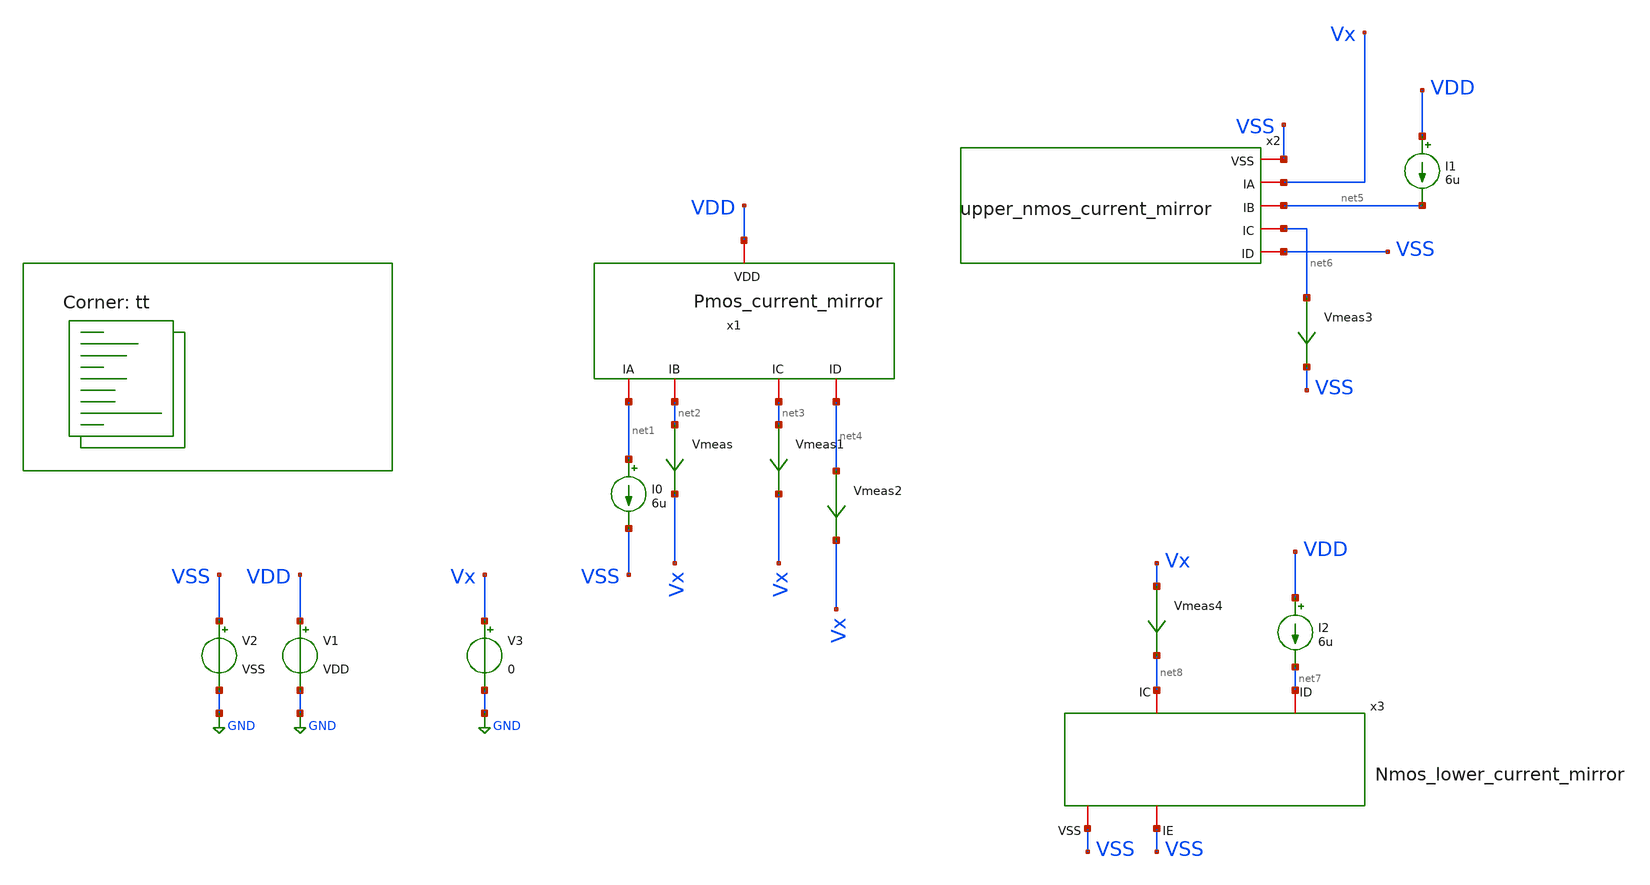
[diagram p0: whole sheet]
** sch_path: Learning/single_ended_amplifiers/VA001_series/Design_and_Analysis_of_Two-Stage_CMOS_Operational_Amplifier_for_Fluorescence_Signal_Processing_sky130_5V/amplifier_design/test.sch
**.subckt test
V1 VDD GND VDD
V2 VSS GND VSS
x1 VDD net1 net2 net3 net4 Pmos_current_mirror
I0 net1 VSS 6u
V3 Vx GND 0
Vmeas net2 Vx 0
.save i(vmeas)
Vmeas1 net3 Vx 0
.save i(vmeas1)
Vmeas2 net4 Vx 0
.save i(vmeas2)
I1 VDD net5 6u
Vmeas3 net6 VSS 0
.save i(vmeas3)
x2 VSS Vx net5 net6 VSS upper_nmos_current_mirror
x3 VSS net8 net7 VSS Nmos_lower_current_mirror
I2 VDD net7 6u
Vmeas4 Vx net8 0
.save i(vmeas4)
**** begin user architecture code
.lib $::SKYWATER_MODELS/sky130.lib.spice tt

.Temp 27
.param VDD = 5
.param VSS = 0
.param VCM = 2.5
.param VCM_NEG={-VCM}
.param V_OFF = -880.69u
.param CL = 3p


.control
save all

dc V3 0 5 0.001
plot i(Vmeas4)

.endc



.subckt upper_nmos_current_mirror VSS IA IB IC ID
X0 VSS VSS IB VSS sky130_fd_pr__nfet_g5v0d10v5 ad=0.29 pd=2.58 as=0.145 ps=1.29 w=1 l=2
X1 VSS VSS ID VSS sky130_fd_pr__nfet_g5v0d10v5 ad=0.145 pd=1.29 as=0.145 ps=1.29 w=1 l=2
X2 IA IB IC VSS sky130_fd_pr__nfet_g5v0d10v5 ad=0.145 pd=1.29 as=0.145 ps=1.29 w=1 l=2
X3 IB IB ID VSS sky130_fd_pr__nfet_g5v0d10v5 ad=0.145 pd=1.29 as=0.145 ps=1.29 w=1 l=2
X4 VSS VSS IA VSS sky130_fd_pr__nfet_g5v0d10v5 ad=0.145 pd=1.29 as=0.145 ps=1.29 w=1 l=2
X5 IA VSS VSS VSS sky130_fd_pr__nfet_g5v0d10v5 ad=0.145 pd=1.29 as=0.145 ps=1.29 w=1 l=2
X6 ID IB IB VSS sky130_fd_pr__nfet_g5v0d10v5 ad=0.145 pd=1.29 as=0.145 ps=1.29 w=1 l=2
X7 IB VSS VSS VSS sky130_fd_pr__nfet_g5v0d10v5 ad=0.145 pd=1.29 as=0.29 ps=2.58 w=1 l=2
X8 IC IB IA VSS sky130_fd_pr__nfet_g5v0d10v5 ad=0.145 pd=1.29 as=0.145 ps=1.29 w=1 l=2
X9 ID VSS VSS VSS sky130_fd_pr__nfet_g5v0d10v5 ad=0.145 pd=1.29 as=0.145 ps=1.29 w=1 l=2
X10 VSS VSS IB VSS sky130_fd_pr__nfet_g5v0d10v5 ad=2.32 pd=20.64 as=1.16 ps=10.32 w=1 l=2
X11 VSS VSS ID VSS sky130_fd_pr__nfet_g5v0d10v5 ad=0 pd=0 as=1.16 ps=10.32 w=1 l=2
X12 IA IB IC VSS sky130_fd_pr__nfet_g5v0d10v5 ad=1.16 pd=10.32 as=0.58 ps=5.16 w=1 l=2
X13 IB IB ID VSS sky130_fd_pr__nfet_g5v0d10v5 ad=0 pd=0 as=0 ps=0 w=1 l=2
X14 VSS VSS IA VSS sky130_fd_pr__nfet_g5v0d10v5 ad=0 pd=0 as=0 ps=0 w=1 l=2
X15 IA VSS VSS VSS sky130_fd_pr__nfet_g5v0d10v5 ad=0 pd=0 as=0 ps=0 w=1 l=2
X16 ID IB IB VSS sky130_fd_pr__nfet_g5v0d10v5 ad=0 pd=0 as=0 ps=0 w=1 l=2
X17 IB VSS VSS VSS sky130_fd_pr__nfet_g5v0d10v5 ad=0 pd=0 as=0 ps=0 w=1 l=2
X18 IC IB IA VSS sky130_fd_pr__nfet_g5v0d10v5 ad=0 pd=0 as=0 ps=0 w=1 l=2
X19 ID VSS VSS VSS sky130_fd_pr__nfet_g5v0d10v5 ad=0 pd=0 as=0 ps=0 w=1 l=2
C0 IB VSS 2.32803f
C1 VSS 0 7.91723f
C2 IB 0 7.85092f
.ends




.subckt pmos_current_mirror VDD IA IB IC ID
X0 IA VDD VDD VDD sky130_fd_pr__pfet_g5v0d10v5 ad=0.29 pd=2.58 as=0.29 ps=2.58 w=1 l=2.2
X1 IA VDD VDD VDD sky130_fd_pr__pfet_g5v0d10v5 ad=1.16003 pd=10.325 as=9.86003 ps=87.725 w=1 l=2.2
X2 VDD VDD VDD VDD sky130_fd_pr__pfet_g5v0d10v5 ad=0 pd=0 as=0 ps=0 w=1 l=2.2
X3 VDD IA IA VDD sky130_fd_pr__pfet_g5v0d10v5 ad=0.29 pd=2.58 as=0.29 ps=2.58 w=1 l=2
X4 VDD IA IA VDD sky130_fd_pr__pfet_g5v0d10v5 ad=0 pd=0 as=0 ps=0 w=1 l=2
X5 VDD IA IA VDD sky130_fd_pr__pfet_g5v0d10v5 ad=0 pd=0 as=0 ps=0 w=1 l=2
X6 VDD IA IA VDD sky130_fd_pr__pfet_g5v0d10v5 ad=0 pd=0 as=0 ps=0 w=1 l=2
X7 VDD IA IB VDD sky130_fd_pr__pfet_g5v0d10v5 ad=0.29 pd=2.58 as=0.145 ps=1.29 w=1 l=2.2
X8 IB IA VDD VDD sky130_fd_pr__pfet_g5v0d10v5 ad=0.145 pd=1.29 as=0.29 ps=2.58 w=1 l=2.2
X9 VDD IA ID VDD sky130_fd_pr__pfet_g5v0d10v5 ad=0.29 pd=2.58 as=0.145 ps=1.29 w=1 l=2.2
X10 ID IA VDD VDD sky130_fd_pr__pfet_g5v0d10v5 ad=0.145 pd=1.29 as=0.145 ps=1.29 w=1 l=2.2
X11 VDD IA ID VDD sky130_fd_pr__pfet_g5v0d10v5 ad=0.145 pd=1.29 as=0.145 ps=1.29 w=1 l=2.2
X12 ID IA VDD VDD sky130_fd_pr__pfet_g5v0d10v5 ad=0.145 pd=1.29 as=0.29 ps=2.58 w=1 l=2.2
X13 VDD IA IB VDD sky130_fd_pr__pfet_g5v0d10v5 ad=0 pd=0 as=0.58 ps=5.16 w=1 l=2.2
X14 IB IA VDD VDD sky130_fd_pr__pfet_g5v0d10v5 ad=0 pd=0 as=0 ps=0 w=1 l=2.2
X15 VDD IA IC VDD sky130_fd_pr__pfet_g5v0d10v5 ad=0 pd=0 as=2.32 ps=20.64 w=1 l=2.2
X16 IC IA VDD VDD sky130_fd_pr__pfet_g5v0d10v5 ad=0 pd=0 as=0 ps=0 w=1 l=2.2
X17 VDD IA IC VDD sky130_fd_pr__pfet_g5v0d10v5 ad=0 pd=0 as=0 ps=0 w=1 l=2.2
X18 IC IA VDD VDD sky130_fd_pr__pfet_g5v0d10v5 ad=0 pd=0 as=0 ps=0 w=1 l=2.2
X19 VDD IA ID VDD sky130_fd_pr__pfet_g5v0d10v5 ad=0 pd=0 as=4.64 ps=41.28 w=1 l=2.2
X20 ID IA VDD VDD sky130_fd_pr__pfet_g5v0d10v5 ad=0 pd=0 as=0 ps=0 w=1 l=2.2
X21 VDD IA ID VDD sky130_fd_pr__pfet_g5v0d10v5 ad=0 pd=0 as=0 ps=0 w=1 l=2.2
X22 ID IA VDD VDD sky130_fd_pr__pfet_g5v0d10v5 ad=0 pd=0 as=0 ps=0 w=1 l=2.2
X23 VDD IA ID VDD sky130_fd_pr__pfet_g5v0d10v5 ad=0 pd=0 as=0 ps=0 w=1 l=2.2
X24 ID IA VDD VDD sky130_fd_pr__pfet_g5v0d10v5 ad=0 pd=0 as=0 ps=0 w=1 l=2.2
X25 VDD IA ID VDD sky130_fd_pr__pfet_g5v0d10v5 ad=0 pd=0 as=0 ps=0 w=1 l=2.2
X26 ID IA VDD VDD sky130_fd_pr__pfet_g5v0d10v5 ad=0 pd=0 as=0 ps=0 w=1 l=2.2
X27 VDD IA ID VDD sky130_fd_pr__pfet_g5v0d10v5 ad=0 pd=0 as=0 ps=0 w=1 l=2.2
X28 ID IA VDD VDD sky130_fd_pr__pfet_g5v0d10v5 ad=0 pd=0 as=0 ps=0 w=1 l=2.2
X29 VDD IA ID VDD sky130_fd_pr__pfet_g5v0d10v5 ad=0 pd=0 as=0 ps=0 w=1 l=2.2
X30 ID IA VDD VDD sky130_fd_pr__pfet_g5v0d10v5 ad=0 pd=0 as=0 ps=0 w=1 l=2.2
X31 VDD IA IC VDD sky130_fd_pr__pfet_g5v0d10v5 ad=0 pd=0 as=0 ps=0 w=1 l=2.2
X32 IC IA VDD VDD sky130_fd_pr__pfet_g5v0d10v5 ad=0 pd=0 as=0 ps=0 w=1 l=2.2
X33 VDD IA IC VDD sky130_fd_pr__pfet_g5v0d10v5 ad=0 pd=0 as=0 ps=0 w=1 l=2.2
X34 IC IA VDD VDD sky130_fd_pr__pfet_g5v0d10v5 ad=0 pd=0 as=0 ps=0 w=1 l=2.2
X35 VDD IA ID VDD sky130_fd_pr__pfet_g5v0d10v5 ad=0 pd=0 as=0 ps=0 w=1 l=2.2
X36 ID IA VDD VDD sky130_fd_pr__pfet_g5v0d10v5 ad=0 pd=0 as=0 ps=0 w=1 l=2.2
X37 VDD IA ID VDD sky130_fd_pr__pfet_g5v0d10v5 ad=0 pd=0 as=0 ps=0 w=1 l=2.2
X38 ID IA VDD VDD sky130_fd_pr__pfet_g5v0d10v5 ad=0 pd=0 as=0 ps=0 w=1 l=2.2
X39 VDD IA IC VDD sky130_fd_pr__pfet_g5v0d10v5 ad=0 pd=0 as=0 ps=0 w=1 l=2.2
X40 IC IA VDD VDD sky130_fd_pr__pfet_g5v0d10v5 ad=0 pd=0 as=0 ps=0 w=1 l=2.2
X41 VDD IA IC VDD sky130_fd_pr__pfet_g5v0d10v5 ad=0 pd=0 as=0 ps=0 w=1 l=2.2
X42 IC IA VDD VDD sky130_fd_pr__pfet_g5v0d10v5 ad=0 pd=0 as=0 ps=0 w=1 l=2.2
X43 VDD IA ID VDD sky130_fd_pr__pfet_g5v0d10v5 ad=0 pd=0 as=0 ps=0 w=1 l=2.2
X44 ID IA VDD VDD sky130_fd_pr__pfet_g5v0d10v5 ad=0 pd=0 as=0 ps=0 w=1 l=2.2
X45 VDD IA ID VDD sky130_fd_pr__pfet_g5v0d10v5 ad=0 pd=0 as=0 ps=0 w=1 l=2.2
X46 ID IA VDD VDD sky130_fd_pr__pfet_g5v0d10v5 ad=0 pd=0 as=0 ps=0 w=1 l=2.2
X47 VDD IA ID VDD sky130_fd_pr__pfet_g5v0d10v5 ad=0 pd=0 as=0 ps=0 w=1 l=2.2
X48 ID IA VDD VDD sky130_fd_pr__pfet_g5v0d10v5 ad=0 pd=0 as=0 ps=0 w=1 l=2.2
X49 VDD IA ID VDD sky130_fd_pr__pfet_g5v0d10v5 ad=0 pd=0 as=0 ps=0 w=1 l=2.2
X50 ID IA VDD VDD sky130_fd_pr__pfet_g5v0d10v5 ad=0 pd=0 as=0 ps=0 w=1 l=2.2
X51 VDD IA ID VDD sky130_fd_pr__pfet_g5v0d10v5 ad=0 pd=0 as=0 ps=0 w=1 l=2.2
X52 ID IA VDD VDD sky130_fd_pr__pfet_g5v0d10v5 ad=0 pd=0 as=0 ps=0 w=1 l=2.2
X53 VDD IA ID VDD sky130_fd_pr__pfet_g5v0d10v5 ad=0 pd=0 as=0 ps=0 w=1 l=2.2
X54 ID IA VDD VDD sky130_fd_pr__pfet_g5v0d10v5 ad=0 pd=0 as=0 ps=0 w=1 l=2.2
X55 VDD IA IC VDD sky130_fd_pr__pfet_g5v0d10v5 ad=0 pd=0 as=0 ps=0 w=1 l=2.2
X56 IC IA VDD VDD sky130_fd_pr__pfet_g5v0d10v5 ad=0 pd=0 as=0 ps=0 w=1 l=2.2
X57 VDD IA IC VDD sky130_fd_pr__pfet_g5v0d10v5 ad=0 pd=0 as=0 ps=0 w=1 l=2.2
X58 IC IA VDD VDD sky130_fd_pr__pfet_g5v0d10v5 ad=0 pd=0 as=0 ps=0 w=1 l=2.2
X59 IA VDD VDD VDD sky130_fd_pr__pfet_g5v0d10v5 ad=0 pd=0 as=0 ps=0 w=1 l=2.2
X60 IA VDD VDD VDD sky130_fd_pr__pfet_g5v0d10v5 ad=0 pd=0 as=0 ps=0 w=1 l=2.2
X61 VDD VDD VDD VDD sky130_fd_pr__pfet_g5v0d10v5 ad=0 pd=0 as=0 ps=0 w=1 l=2.2
C0 IC VDD 2.16179f
C1 IC IA 3.02042f
C2 VDD IA 38.77541f
C3 IC ID 3.30185f
C4 VDD ID 2.46903f
C5 IA ID 3.42756f
C6 ID VSUBS 2.96362f
C7 IA VSUBS 16.42313f
C8 VDD VSUBS 77.69173f
.ends


.subckt Nmos_lower_current_mirror VSS IC ID IE
X0 IC VSS VSS VSS sky130_fd_pr__nfet_g5v0d10v5 ad=0.29 pd=2.58 as=0.29 ps=2.58 w=1 l=3.2
X1 ID VSS VSS VSS sky130_fd_pr__nfet_g5v0d10v5 ad=1.16003 pd=10.325 as=2.32002 ps=20.645 w=1 l=3.2
X2 IC VSS VSS VSS sky130_fd_pr__nfet_g5v0d10v5 ad=2.90002 pd=25.805 as=0 ps=0 w=1 l=3.2
X3 ID VSS VSS VSS sky130_fd_pr__nfet_g5v0d10v5 ad=0 pd=0 as=0 ps=0 w=1 l=3.2
X4 ID VSS VSS VSS sky130_fd_pr__nfet_g5v0d10v5 ad=0 pd=0 as=0 ps=0 w=1 l=3.2
X5 VSS ID ID VSS sky130_fd_pr__nfet_g5v0d10v5 ad=0.29 pd=2.58 as=0.29 ps=2.58 w=1 l=3.2
X6 IC VSS VSS VSS sky130_fd_pr__nfet_g5v0d10v5 ad=0 pd=0 as=0 ps=0 w=1 l=3.2
X7 VSS ID ID VSS sky130_fd_pr__nfet_g5v0d10v5 ad=0 pd=0 as=0 ps=0 w=1 l=3.2
X8 ID VSS VSS VSS sky130_fd_pr__nfet_g5v0d10v5 ad=0 pd=0 as=0 ps=0 w=1 l=3.2
X9 IC VSS VSS VSS sky130_fd_pr__nfet_g5v0d10v5 ad=0 pd=0 as=0 ps=0 w=1 l=3.2
X10 IE ID IC VSS sky130_fd_pr__nfet_g5v0d10v5 ad=0.145 pd=1.29 as=0.29 ps=2.58 w=1 l=3.2
X11 IC ID IE VSS sky130_fd_pr__nfet_g5v0d10v5 ad=0.29 pd=2.58 as=0.145 ps=1.29 w=1 l=3.2
X12 VSS ID ID VSS sky130_fd_pr__nfet_g5v0d10v5 ad=0 pd=0 as=0 ps=0 w=1 l=3.2
X13 VSS ID ID VSS sky130_fd_pr__nfet_g5v0d10v5 ad=0 pd=0 as=0 ps=0 w=1 l=3.2
X14 IE ID IC VSS sky130_fd_pr__nfet_g5v0d10v5 ad=2.32 pd=20.64 as=0 ps=0 w=1 l=3.2
X15 IC ID IE VSS sky130_fd_pr__nfet_g5v0d10v5 ad=0 pd=0 as=0 ps=0 w=1 l=3.2
X16 IE ID IC VSS sky130_fd_pr__nfet_g5v0d10v5 ad=0 pd=0 as=0 ps=0 w=1 l=3.2
X17 IC ID IE VSS sky130_fd_pr__nfet_g5v0d10v5 ad=0 pd=0 as=0 ps=0 w=1 l=3.2
X18 IE ID IC VSS sky130_fd_pr__nfet_g5v0d10v5 ad=0 pd=0 as=0 ps=0 w=1 l=3.2
X19 IC ID IE VSS sky130_fd_pr__nfet_g5v0d10v5 ad=0 pd=0 as=0 ps=0 w=1 l=3.2
X20 IE ID IC VSS sky130_fd_pr__nfet_g5v0d10v5 ad=0 pd=0 as=0 ps=0 w=1 l=3.2
X21 IC ID IE VSS sky130_fd_pr__nfet_g5v0d10v5 ad=0 pd=0 as=0 ps=0 w=1 l=3.2
X22 IE ID IC VSS sky130_fd_pr__nfet_g5v0d10v5 ad=0 pd=0 as=0 ps=0 w=1 l=3.2
X23 IC ID IE VSS sky130_fd_pr__nfet_g5v0d10v5 ad=0 pd=0 as=0 ps=0 w=1 l=3.2
X24 IE ID IC VSS sky130_fd_pr__nfet_g5v0d10v5 ad=0 pd=0 as=0 ps=0 w=1 l=3.2
X25 IC ID IE VSS sky130_fd_pr__nfet_g5v0d10v5 ad=0 pd=0 as=0 ps=0 w=1 l=3.2
X26 IE ID IC VSS sky130_fd_pr__nfet_g5v0d10v5 ad=0 pd=0 as=0 ps=0 w=1 l=3.2
X27 IC ID IE VSS sky130_fd_pr__nfet_g5v0d10v5 ad=0 pd=0 as=0 ps=0 w=1 l=3.2
C0 IE IC 3.21167f
C1 ID IC 2.55348f
C2 VSS ID 6.7579f
C3 IE 0 2.10306f
C4 ID 0 21.8586f
C5 VSS 0 2.30348f
C6 IC 0 2.30032f
.ends



**** end user architecture code
**.ends

* expanding   symbol:
*+  Sky130A/Learning/Design_of_Two-Stage_CMOS_Operational_Amplifier_for_Fluorescence_Signal_Processing_5V/Pmos_current_mirror.sym # of pins=5
** sym_path: Learning/single_ended_amplifiers/Design_and_Analysis_of_Two-Stage_CMOS_Operational_Amplifier_for_Fluorescence_Signal_Processing_sky130_5V/klayout_layout/Pmos_current_mirror.sym
** sch_path: Learning/single_ended_amplifiers/Design_and_Analysis_of_Two-Stage_CMOS_Operational_Amplifier_for_Fluorescence_Signal_Processing_sky130_5V/klayout_layout/Pmos_current_mirror.sch
.subckt Pmos_current_mirror VDD IA IB IC ID
*.iopin VDD
*.iopin IA
*.iopin IB
*.iopin IC
*.iopin ID
XM2 IB IA VDD VDD sky130_fd_pr__pfet_g5v0d10v5 L=2.2 W='1 * 2 ' nf=2 ad='int((2 + 1)/2) * 1 * 0.29' as='int((2 + 2)/2) * 1 * 0.29'
+ pd='2*int((2 + 1)/2) * (1 + 0.29)' ps='2*int((2 + 2)/2) * (1 + 0.29)' nrd='0.29 / 1 / 2 ' nrs='0.29 / 1 / 2 '
+ sa=0 sb=0 sd=0 mult=2 m=2
XM3 IA IA VDD VDD sky130_fd_pr__pfet_g5v0d10v5 L=2.2 W='1 * 2 ' nf=2 ad='int((2 + 1)/2) * 1 * 0.29' as='int((2 + 2)/2) * 1 * 0.29'
+ pd='2*int((2 + 1)/2) * (1 + 0.29)' ps='2*int((2 + 2)/2) * (1 + 0.29)' nrd='0.29 / 1 / 2 ' nrs='0.29 / 1 / 2 '
+ sa=0 sb=0 sd=0 mult=2 m=2
XM4 IC IA VDD VDD sky130_fd_pr__pfet_g5v0d10v5 L=2.2 W='1 * 2 ' nf=2 ad='int((2 + 1)/2) * 1 * 0.29' as='int((2 + 2)/2) * 1 * 0.29'
+ pd='2*int((2 + 1)/2) * (1 + 0.29)' ps='2*int((2 + 2)/2) * (1 + 0.29)' nrd='0.29 / 1 / 2 ' nrs='0.29 / 1 / 2 '
+ sa=0 sb=0 sd=0 mult=8 m=8
XM7 ID IA VDD VDD sky130_fd_pr__pfet_g5v0d10v5 L=2.2 W='1 * 2 ' nf=2 ad='int((2 + 1)/2) * 1 * 0.29' as='int((2 + 2)/2) * 1 * 0.29'
+ pd='2*int((2 + 1)/2) * (1 + 0.29)' ps='2*int((2 + 2)/2) * (1 + 0.29)' nrd='0.29 / 1 / 2 ' nrs='0.29 / 1 / 2 '
+ sa=0 sb=0 sd=0 mult=16 m=16
XM1 IA VDD VDD VDD sky130_fd_pr__pfet_g5v0d10v5 L=2.2 W='1 * 1 ' nf=1 ad='int((1 + 1)/2) * 1 * 0.29'
+ as='int((1 + 2)/2) * 1 * 0.29' pd='2*int((1 + 1)/2) * (1 + 0.29)' ps='2*int((1 + 2)/2) * (1 + 0.29)'
+ nrd='0.29 / 1 / 1 ' nrs='0.29 / 1 / 1 ' sa=0 sb=0 sd=0 mult=4 m=4
XM5 VDD VDD VDD VDD sky130_fd_pr__pfet_g5v0d10v5 L=2.2 W='1 * 1 ' nf=1 ad='int((1 + 1)/2) * 1 * 0.29'
+ as='int((1 + 2)/2) * 1 * 0.29' pd='2*int((1 + 1)/2) * (1 + 0.29)' ps='2*int((1 + 2)/2) * (1 + 0.29)'
+ nrd='0.29 / 1 / 1 ' nrs='0.29 / 1 / 1 ' sa=0 sb=0 sd=0 mult=2 m=2
.ends

.GLOBAL GND
.end
